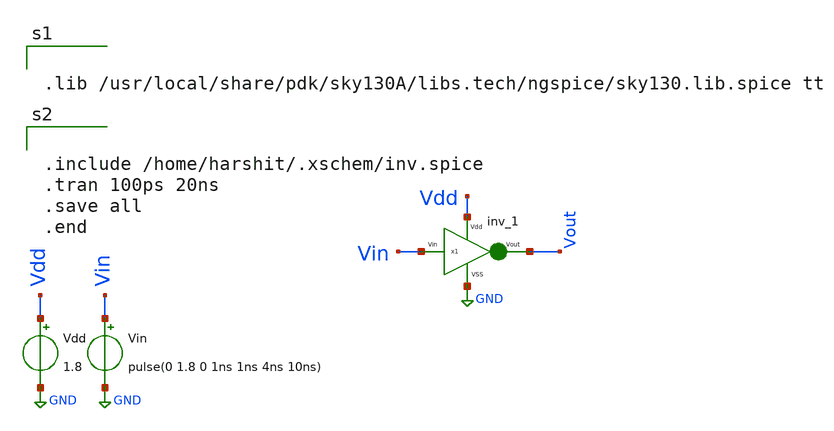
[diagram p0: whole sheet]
** sch_path: xschem files/inv_tran.sch
**.subckt inv_tran
Vin Vin GND pulse(0 1.8 0 1ns 1ns 4ns 10ns)
Vdd Vdd GND 1.8
x1 Vdd Vout Vin GND inv_1
**** begin user architecture code


.lib /usr/local/share/pdk/sky130A/libs.tech/ngspice/sky130.lib.spice tt



.include /home/harshit/.xschem/inv.spice
.tran 100ps 20ns
.save all
.end

**** end user architecture code
**.ends

* expanding   symbol:  /home/harshit/.xschem/inv_1.sym # of pins=4
** sym_path: xschem files/inv_1.sym
** sch_path: xschem files/inv_1.sch
.subckt inv_1 Vdd Vout Vin VSS
*.ipin Vdd
*.ipin VSS
*.opin Vout
*.ipin Vin
XM1 Vout Vin VSS VSS sky130_fd_pr__nfet_01v8 L=0.15 W=1.05 nf=1 ad='int((nf+1)/2) * W/nf * 0.29' as='int((nf+2)/2) * W/nf * 0.29'
+ pd='2*int((nf+1)/2) * (W/nf + 0.29)' ps='2*int((nf+2)/2) * (W/nf + 0.29)' nrd='0.29 / W' nrs='0.29 / W'
+ sa=0 sb=0 sd=0 mult=1 m=1
XM2 Vout Vin Vdd Vdd sky130_fd_pr__pfet_01v8 L=0.15 W=2.1 nf=1 ad='int((nf+1)/2) * W/nf * 0.29' as='int((nf+2)/2) * W/nf * 0.29'
+ pd='2*int((nf+1)/2) * (W/nf + 0.29)' ps='2*int((nf+2)/2) * (W/nf + 0.29)' nrd='0.29 / W' nrs='0.29 / W'
+ sa=0 sb=0 sd=0 mult=1 m=1
.ends

.GLOBAL GND
.end
